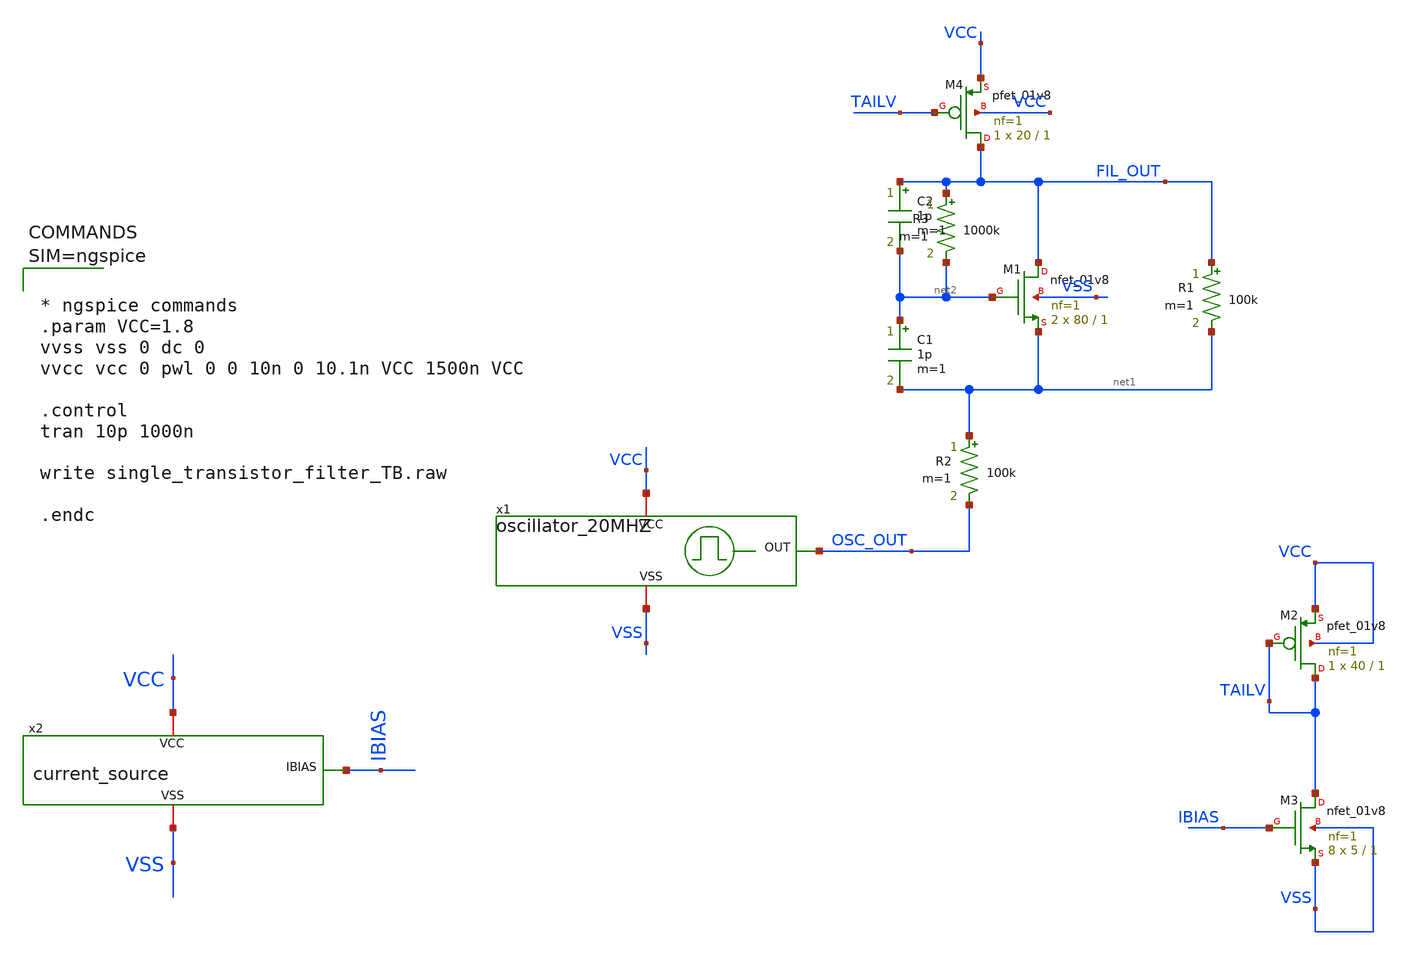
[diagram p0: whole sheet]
** sch_path: xschem/single_transistor_filter_tb.sch
**.subckt single_transistor_filter_tb
XM1 FIL_OUT net2 net1 VSS sky130_fd_pr__nfet_01v8 L=1 W=80 nf=1 ad='int((nf+1)/2) * W/nf * 0.29' as='int((nf+2)/2) * W/nf * 0.29'
+ pd='2*int((nf+1)/2) * (W/nf + 0.29)' ps='2*int((nf+2)/2) * (W/nf + 0.29)' nrd='0.29 / W' nrs='0.29 / W'
+ sa=0 sb=0 sd=0 mult=2 m=2
C1 net2 net1 1p m=1
C2 FIL_OUT net2 1p m=1
R1 FIL_OUT net1 100k m=1
x1 VCC OSC_OUT VSS oscillator_20MHZ
R2 net1 OSC_OUT 100k m=1
x2 VCC VSS IBIAS current_source
XM3 TAILV IBIAS VSS VSS sky130_fd_pr__nfet_01v8 L=1 W=5 nf=1 ad='int((nf+1)/2) * W/nf * 0.29' as='int((nf+2)/2) * W/nf * 0.29'
+ pd='2*int((nf+1)/2) * (W/nf + 0.29)' ps='2*int((nf+2)/2) * (W/nf + 0.29)' nrd='0.29 / W' nrs='0.29 / W'
+ sa=0 sb=0 sd=0 mult=8 m=8
XM2 TAILV TAILV VCC VCC sky130_fd_pr__pfet_01v8 L=1 W=40 nf=1 ad='int((nf+1)/2) * W/nf * 0.29' as='int((nf+2)/2) * W/nf * 0.29'
+ pd='2*int((nf+1)/2) * (W/nf + 0.29)' ps='2*int((nf+2)/2) * (W/nf + 0.29)' nrd='0.29 / W' nrs='0.29 / W'
+ sa=0 sb=0 sd=0 mult=1 m=1
XM4 FIL_OUT TAILV VCC VCC sky130_fd_pr__pfet_01v8 L=1 W=20 nf=1 ad='int((nf+1)/2) * W/nf * 0.29' as='int((nf+2)/2) * W/nf * 0.29'
+ pd='2*int((nf+1)/2) * (W/nf + 0.29)' ps='2*int((nf+2)/2) * (W/nf + 0.29)' nrd='0.29 / W' nrs='0.29 / W'
+ sa=0 sb=0 sd=0 mult=1 m=1
R3 FIL_OUT net2 1000k m=1
**** begin user architecture code

** opencircuitdesign pdks install
.lib $::SKYWATER_MODELS/sky130.lib.spice tt





* ngspice commands
.param VCC=1.8
vvss vss 0 dc 0
vvcc vcc 0 pwl 0 0 10n 0 10.1n VCC 1500n VCC

.control
tran 10p 1000n

write single_transistor_filter_TB.raw

.endc




**** end user architecture code
**.ends

* expanding   symbol:  oscillator_20MHZ.sym # of pins=3
** sym_path: xschem/oscillator_20MHZ.sym
** sch_path: xschem/oscillator_20MHZ.sch
.subckt oscillator_20MHZ VCC OUT VSS
*.iopin VCC
*.iopin VSS
*.opin OUT
x1[30] INI[29] OUT_INI VCC VSS inverter
x1[29] INI[28] INI[29] VCC VSS inverter
x1[28] INI[27] INI[28] VCC VSS inverter
x1[27] INI[26] INI[27] VCC VSS inverter
x1[26] INI[25] INI[26] VCC VSS inverter
x1[25] INI[24] INI[25] VCC VSS inverter
x1[24] INI[23] INI[24] VCC VSS inverter
x1[23] INI[22] INI[23] VCC VSS inverter
x1[22] INI[21] INI[22] VCC VSS inverter
x1[21] INI[20] INI[21] VCC VSS inverter
x1[20] INI[19] INI[20] VCC VSS inverter
x1[19] INI[18] INI[19] VCC VSS inverter
x1[18] INI[17] INI[18] VCC VSS inverter
x1[17] INI[16] INI[17] VCC VSS inverter
x1[16] INI[15] INI[16] VCC VSS inverter
x1[15] INI[14] INI[15] VCC VSS inverter
x1[14] INI[13] INI[14] VCC VSS inverter
x1[13] INI[12] INI[13] VCC VSS inverter
x1[12] INI[11] INI[12] VCC VSS inverter
x1[11] INI[10] INI[11] VCC VSS inverter
x1[10] INI[9] INI[10] VCC VSS inverter
x1[9] INI[8] INI[9] VCC VSS inverter
x1[8] INI[7] INI[8] VCC VSS inverter
x1[7] INI[6] INI[7] VCC VSS inverter
x1[6] INI[5] INI[6] VCC VSS inverter
x1[5] INI[4] INI[5] VCC VSS inverter
x1[4] INI[3] INI[4] VCC VSS inverter
x1[3] INI[2] INI[3] VCC VSS inverter
x1[2] INI[1] INI[2] VCC VSS inverter
x1[1] INI[0] INI[1] VCC VSS inverter
x1[0] OUT_INI INI[0] VCC VSS inverter
x3 OUT OUT_INI VCC VSS inverter
.ends


* expanding   symbol:  current_source.sym # of pins=3
** sym_path: xschem/current_source.sym
** sch_path: xschem/current_source.sch
.subckt current_source VCC VSS IBIAS
*.iopin VCC
*.iopin VSS
*.opin IBIAS
XM3 IBIAS IBIAS VSS VSS sky130_fd_pr__nfet_01v8 L=1 W=40 nf=1 ad='int((nf+1)/2) * W/nf * 0.29' as='int((nf+2)/2) * W/nf * 0.29'
+ pd='2*int((nf+1)/2) * (W/nf + 0.29)' ps='2*int((nf+2)/2) * (W/nf + 0.29)' nrd='0.29 / W' nrs='0.29 / W'
+ sa=0 sb=0 sd=0 mult=1 m=1
XR1 IBIAS VCC sky130_fd_pr__res_generic_po W=0.33 L=12 m=1
.ends


* expanding   symbol:  inverter.sym # of pins=4
** sym_path: xschem/inverter.sym
** sch_path: xschem/inverter.sch
.subckt inverter OUT IN VCC VSS
*.iopin VCC
*.iopin VSS
*.ipin IN
*.opin OUT
XM1 OUT IN net1 VCC sky130_fd_pr__pfet_01v8 L=1 W=2 nf=1 ad='int((nf+1)/2) * W/nf * 0.29' as='int((nf+2)/2) * W/nf * 0.29'
+ pd='2*int((nf+1)/2) * (W/nf + 0.29)' ps='2*int((nf+2)/2) * (W/nf + 0.29)' nrd='0.29 / W' nrs='0.29 / W'
+ sa=0 sb=0 sd=0 mult=1 m=1
XM2 OUT IN net2 VSS sky130_fd_pr__nfet_01v8 L=1 W=1 nf=1 ad='int((nf+1)/2) * W/nf * 0.29' as='int((nf+2)/2) * W/nf * 0.29'
+ pd='2*int((nf+1)/2) * (W/nf + 0.29)' ps='2*int((nf+2)/2) * (W/nf + 0.29)' nrd='0.29 / W' nrs='0.29 / W'
+ sa=0 sb=0 sd=0 mult=1 m=1
XM3 net1 VSS VCC VCC sky130_fd_pr__pfet_01v8 L=1 W=2 nf=1 ad='int((nf+1)/2) * W/nf * 0.29' as='int((nf+2)/2) * W/nf * 0.29'
+ pd='2*int((nf+1)/2) * (W/nf + 0.29)' ps='2*int((nf+2)/2) * (W/nf + 0.29)' nrd='0.29 / W' nrs='0.29 / W'
+ sa=0 sb=0 sd=0 mult=1 m=1
XM4 net2 VCC VSS VSS sky130_fd_pr__nfet_01v8 L=1 W=1 nf=1 ad='int((nf+1)/2) * W/nf * 0.29' as='int((nf+2)/2) * W/nf * 0.29'
+ pd='2*int((nf+1)/2) * (W/nf + 0.29)' ps='2*int((nf+2)/2) * (W/nf + 0.29)' nrd='0.29 / W' nrs='0.29 / W'
+ sa=0 sb=0 sd=0 mult=1 m=1
.ends

.end
